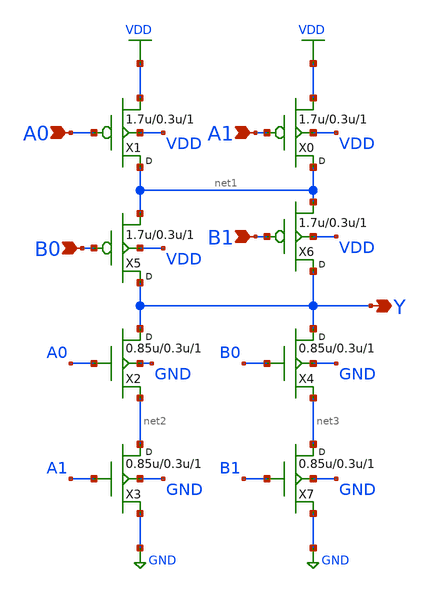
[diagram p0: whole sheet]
** sch_path: gf180mcu_osu_sc_gp9t3v3/cells/aoi22/gf180mcu_osu_sc_gp9t3v3__aoi22_1.sch
**.subckt gf180mcu_osu_sc_gp9t3v3__aoi22_1 A0 A1 B0 B1 Y
*.ipin A0
*.ipin A1
*.ipin B0
*.ipin B1
*.opin Y
X1 net1 A0 VDD VDD pfet_03p3 w=1.7u l=0.3u m=1
X0 net1 A1 VDD VDD pfet_03p3 w=1.7u l=0.3u m=1
X2 Y A0 net2 GND nfet_03p3 w=0.85u l=0.3u m=1
X3 net2 A1 GND GND nfet_03p3 w=0.85u l=0.3u m=1
X4 Y B0 net3 GND nfet_03p3 w=0.85u l=0.3u m=1
X5 Y B0 net1 VDD pfet_03p3 w=1.7u l=0.3u m=1
X6 Y B1 net1 VDD pfet_03p3 w=1.7u l=0.3u m=1
X7 net3 B1 GND GND nfet_03p3 w=0.85u l=0.3u m=1
**.ends
.GLOBAL VDD
.GLOBAL GND
.end
